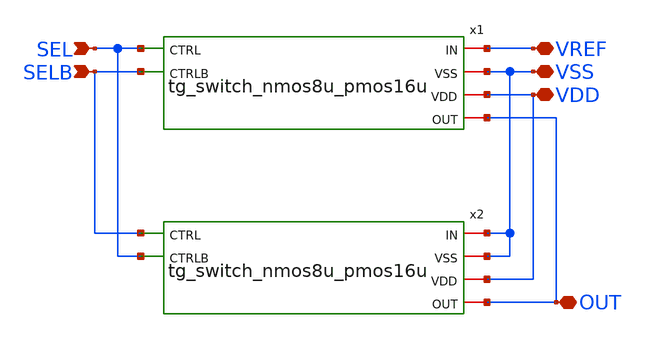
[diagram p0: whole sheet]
** sch_path: designs/libs/core_matchmaker/ref_sel_2to1_nmos8u_pmos16u/ref_sel_2to1_nmos8u_pmos16u.sch
**.subckt ref_sel_2to1_nmos8u_pmos16u VREF VSS VDD OUT SEL SELB
*.iopin VREF
*.iopin VSS
*.iopin VDD
*.iopin OUT
*.ipin SEL
*.ipin SELB
x1 VREF VSS VDD SEL SELB OUT tg_switch_nmos8u_pmos16u
x2 VSS VSS VDD SELB SEL OUT tg_switch_nmos8u_pmos16u
**.ends

* expanding   symbol:  libs/core_matchmaker/tg_switch_nmos8u_pmos16u/tg_switch_nmos8u_pmos16u.sym #
*+ of pins=6
** sym_path: designs/libs/core_matchmaker/tg_switch/tg_switch_nmos8u_pmos16u.sym
** sch_path: designs/libs/core_matchmaker/tg_switch/tg_switch_nmos8u_pmos16u.sch
.subckt tg_switch_nmos8u_pmos16u IN VSS VDD CTRL CTRLB OUT
*.iopin IN
*.iopin OUT
*.iopin VSS
*.iopin VDD
*.ipin CTRL
*.ipin CTRLB
XM1 IN CTRL OUT VSS nfet_03v3 L=0.28u W=8u nf=1 ad='int((nf+1)/2) * W/nf * 0.18u' as='int((nf+2)/2) * W/nf * 0.18u'
+ pd='2*int((nf+1)/2) * (W/nf + 0.18u)' ps='2*int((nf+2)/2) * (W/nf + 0.18u)' nrd='0.18u / W' nrs='0.18u / W'
+ sa=0 sb=0 sd=0 m=1
XM2 IN CTRLB OUT VDD pfet_03v3 L=0.28u W=16u nf=1 ad='int((nf+1)/2) * W/nf * 0.18u' as='int((nf+2)/2) * W/nf * 0.18u'
+ pd='2*int((nf+1)/2) * (W/nf + 0.18u)' ps='2*int((nf+2)/2) * (W/nf + 0.18u)' nrd='0.18u / W' nrs='0.18u / W'
+ sa=0 sb=0 sd=0 m=1
.ends

.end
